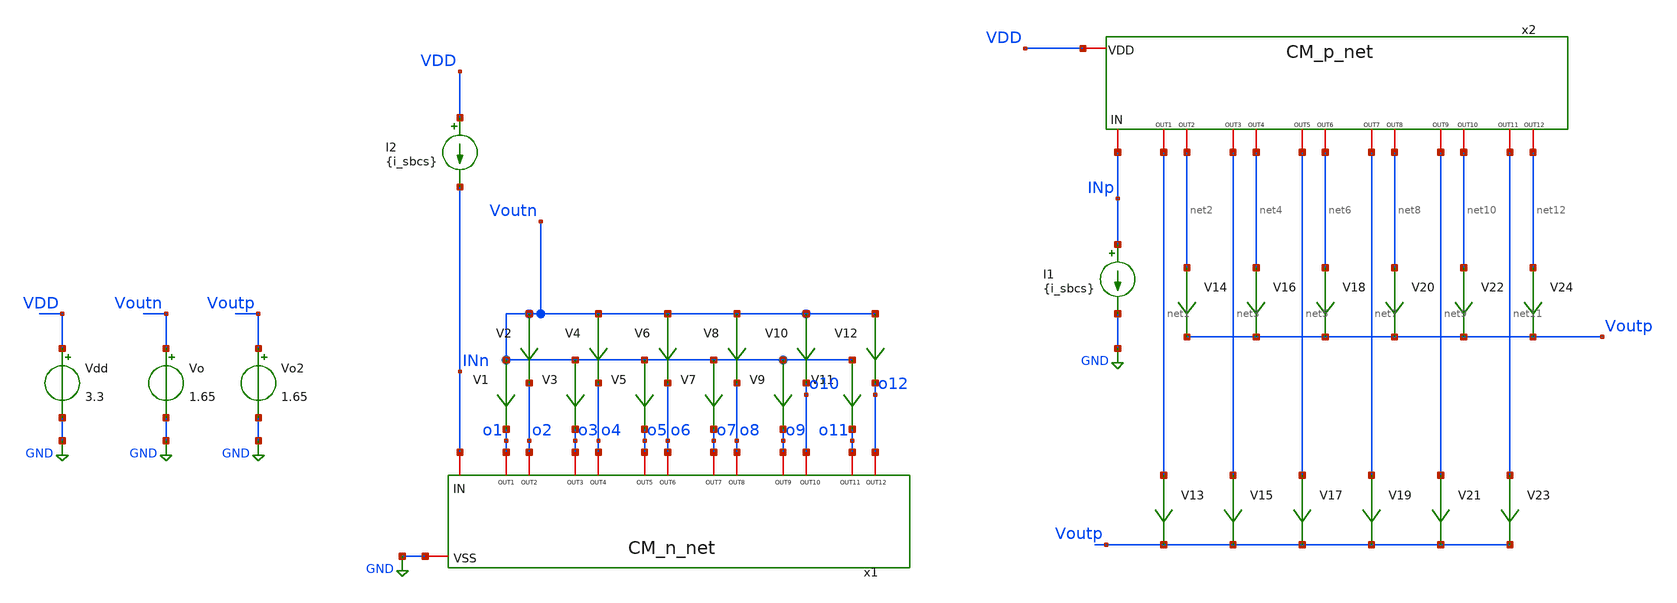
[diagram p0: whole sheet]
** sch_path: TIA_Filter/CurrentMirrors/TB_CM_PR.sch
**.subckt TB_CM_PR
Vdd VDD GND 3.3
V1 Voutn o1 0
.save i(v1)
V2 Voutn o2 0
.save i(v2)
V3 Voutn o3 0
.save i(v3)
V4 Voutn o4 0
.save i(v4)
V5 Voutn o5 0
.save i(v5)
V6 Voutn o6 0
.save i(v6)
V7 Voutn o7 0
.save i(v7)
V8 Voutn o8 0
.save i(v8)
V9 Voutn o9 0
.save i(v9)
V10 Voutn o10 0
.save i(v10)
V11 Voutn o11 0
.save i(v11)
V12 Voutn o12 0
.save i(v12)
Vo Voutn GND 1.65
x1 INn o1 o2 o3 o4 o5 o6 o7 o8 o9 o10 o11 o12 GND CM_n_net
V13 net1 Voutp 0
.save i(v13)
V14 net2 Voutp 0
.save i(v14)
x2 INp net1 net2 net3 net4 net5 net6 net7 net8 net9 net10 net11 net12 VDD CM_p_net
V15 net3 Voutp 0
.save i(v15)
V16 net4 Voutp 0
.save i(v16)
V17 net5 Voutp 0
.save i(v17)
V18 net6 Voutp 0
.save i(v18)
V19 net7 Voutp 0
.save i(v19)
V20 net8 Voutp 0
.save i(v20)
V21 net9 Voutp 0
.save i(v21)
V22 net10 Voutp 0
.save i(v22)
V23 net11 Voutp 0
.save i(v23)
V24 net12 Voutp 0
.save i(v24)
I2 VDD INn {i_sbcs}
I1 INp GND {i_sbcs}
Vo2 Voutp GND 1.65
**** begin user architecture code

.include $::180MCU_MODELS/design.ngspice
.lib $::180MCU_MODELS/sm141064.ngspice typical

.param sw_stat_mismatch=1
.param sw_stat_global=1




.option gmin=1e-15
*.option abstol=1e-18
*.option retol=1e-15

.option klu

.param i_sbcs=1.02n

.control
save all

let sample_num = 0

while sample_num<200
reset

op
remzerovec
write TB_CM_input.raw
wrdata
+ /home/gmaranhao/Desktop/Bracolin/TIA_Filter/CurrentMirrors/plots/CM_input_data/CM_PR_dc_MisMC_3p0.txt i(v1) i(v2) i(v13) i(v14)
set appendwrite

let sample_num = sample_num + 1
end


.endc
.save all


**** end user architecture code
**.ends
.GLOBAL GND
.end
